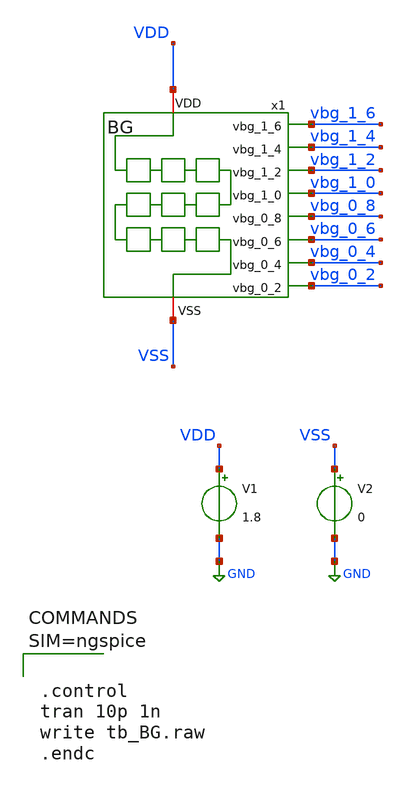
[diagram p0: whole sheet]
** sch_path: xschem/tb_BG.sch
**.subckt tb_BG
V1 VDD GND 1.8
V2 VSS GND 0
x1 vbg_1_6 vbg_1_4 vbg_1_2 vbg_1_0 vbg_0_8 vbg_0_6 vbg_0_4 vbg_0_2 VDD VSS BG
**** begin user architecture code

** opencircuitdesign pdks install
.lib $::SKYWATER_MODELS/sky130.lib.spice tt





.control
tran 10p 1n
write tb_BG.raw
.endc



**** end user architecture code
**.ends

* expanding   symbol:  BG.sym # of pins=10
** sym_path: xschem/BG.sym
** sch_path: xschem/BG.sch
.subckt BG vbg_1_6 vbg_1_4 vbg_1_2 vbg_1_0 vbg_0_8 vbg_0_6 vbg_0_4 vbg_0_2 VDD VSS
*.opin vbg_1_6
*.opin vbg_1_4
*.opin vbg_1_2
*.opin vbg_1_0
*.opin vbg_0_8
*.opin vbg_0_6
*.opin vbg_0_4
*.opin vbg_0_2
*.iopin VDD
*.iopin VSS
XR1 vbg_1_4 vbg_1_6 VSS sky130_fd_pr__res_high_po_0p35 L=1.5 mult=1 m=1
XR0 vbg_1_6 VDD VSS sky130_fd_pr__res_high_po_0p35 L=1.5 mult=1 m=1
XR3 vbg_1_0 vbg_1_2 VSS sky130_fd_pr__res_high_po_0p35 L=1.5 mult=1 m=1
XR2 vbg_1_2 vbg_1_4 VSS sky130_fd_pr__res_high_po_0p35 L=1.5 mult=1 m=1
XR5 vbg_0_6 vbg_0_8 VSS sky130_fd_pr__res_high_po_0p35 L=1.5 mult=1 m=1
XR4 vbg_0_8 vbg_1_0 VSS sky130_fd_pr__res_high_po_0p35 L=1.5 mult=1 m=1
XR6 vbg_0_4 vbg_0_6 VSS sky130_fd_pr__res_high_po_0p35 L=1.5 mult=1 m=1
XR7 vbg_0_2 vbg_0_4 VSS sky130_fd_pr__res_high_po_0p35 L=1.5 mult=1 m=1
XR8 VSS vbg_0_2 VSS sky130_fd_pr__res_high_po_0p35 L=1.5 mult=1 m=1
.ends

.GLOBAL GND
.end
